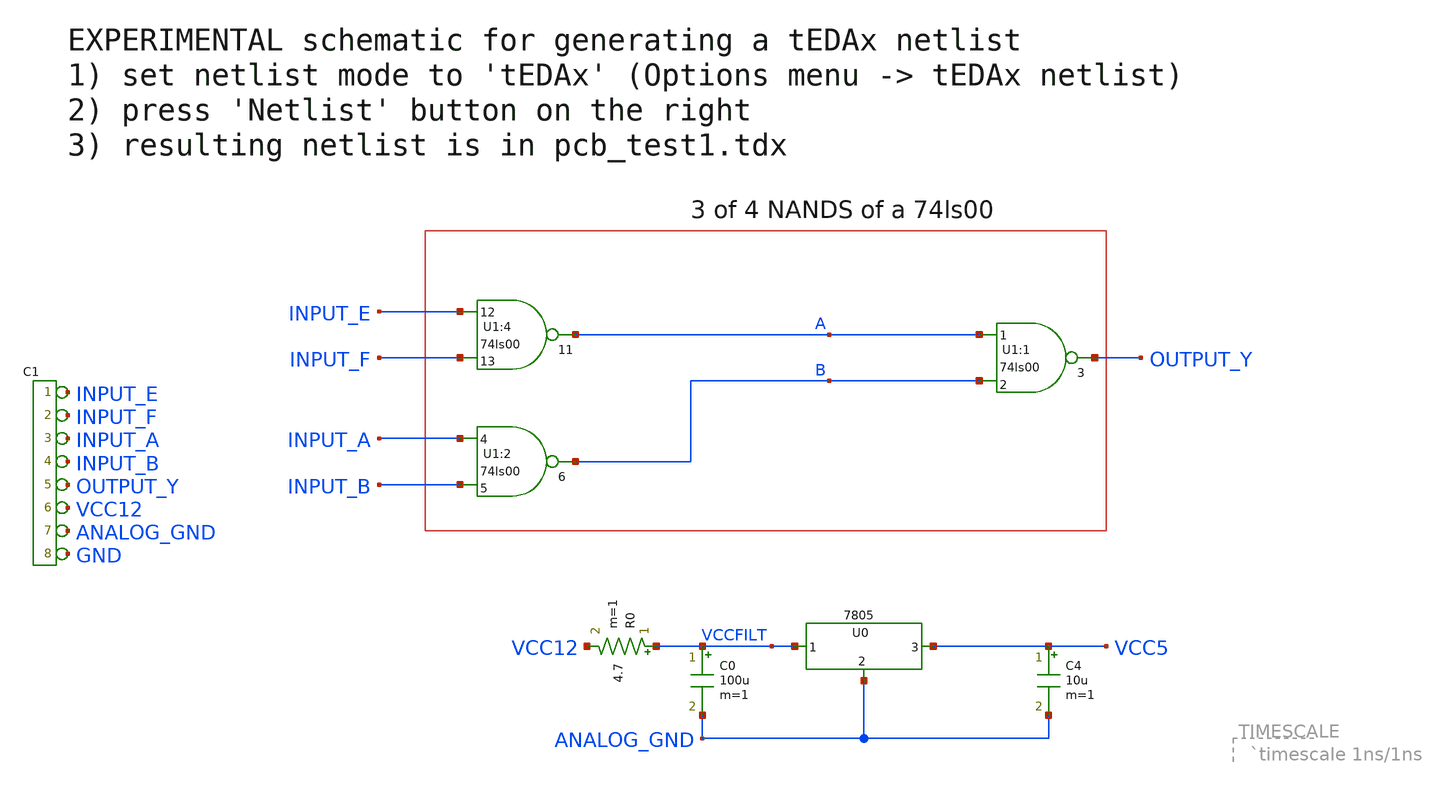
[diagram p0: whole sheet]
** sch_path: xschem-src/xschem_library/pcb/pcb_test1.sch
* Copyright (C) 1998-2026 Stefan Frederik Schippers
* This program is free software; you can redistribute it and/or modify
* it under the terms of the GNU General Public License as published by
* the Free Software Foundation; either version 2 of the License, or
* (at your option) any later version.
* This program is distributed in the hope that it will be useful,
* but WITHOUT ANY WARRANTY; without even the implied warranty of
* MERCHANTABILITY or FITNESS FOR A PARTICULAR PURPOSE.  See the
* GNU General Public License for more details.
* You should have received a copy of the GNU General Public License
* along with this program; if not, write to the Free Software
**.subckt pcb_test1
U1:2 INPUT_A INPUT_B B VCC GND 74ls00
U1:1 A B OUTPUT_Y VCC GND 74ls00
U1:4 INPUT_E INPUT_F A VCC5 GND 74ls00
XU0 VCCFILT ANALOG_GND VCC5 7805
C4 VCC5 ANALOG_GND 10u m=1
R0 VCCFILT VCC12 4.7 m=1
*connector(8,1) ?1 INPUT_E ?1 INPUT_F ?1 INPUT_A ?1 INPUT_B ?1 OUTPUT_Y ?1 VCC12 ?1 ANALOG_GND ?1
*+ GND
C0 VCCFILT ANALOG_GND 100u m=1
**** begin user architecture code

initial begin
  $dumpfile("dumpfile.vcd");
  $dumpvars;
  INPUT_E=0;
  INPUT_F=0;
  INPUT_A=0;
  INPUT_B=0;
  ANALOG_GND=0;
  #10000;
  INPUT_A=1;
  INPUT_B=1;
  #10000;
  INPUT_E=1;
  INPUT_F=1;
  #10000;
  INPUT_F=0;
  #10000;
  INPUT_B=0;
  #10000;
  $finish;
end

assign VCC12=1;



**** end user architecture code
**.ends
.end
